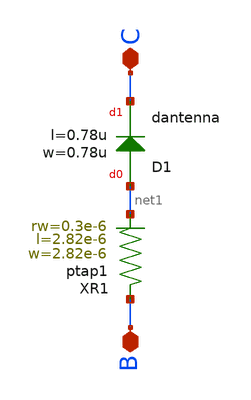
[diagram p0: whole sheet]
** sch_path: ihp-sg13cmos5l/schematic/xschem/sg13_dantenna.sch
**.subckt sg13_dantenna C B
*.iopin C
*.iopin B
XD1 net1 C dantenna l=0.78u w=0.78u
XR1 B net1 ptap1 R=22.61 w=2.82e-6 l=2.82e-6 rw=0.3e-6
**.ends
.end
